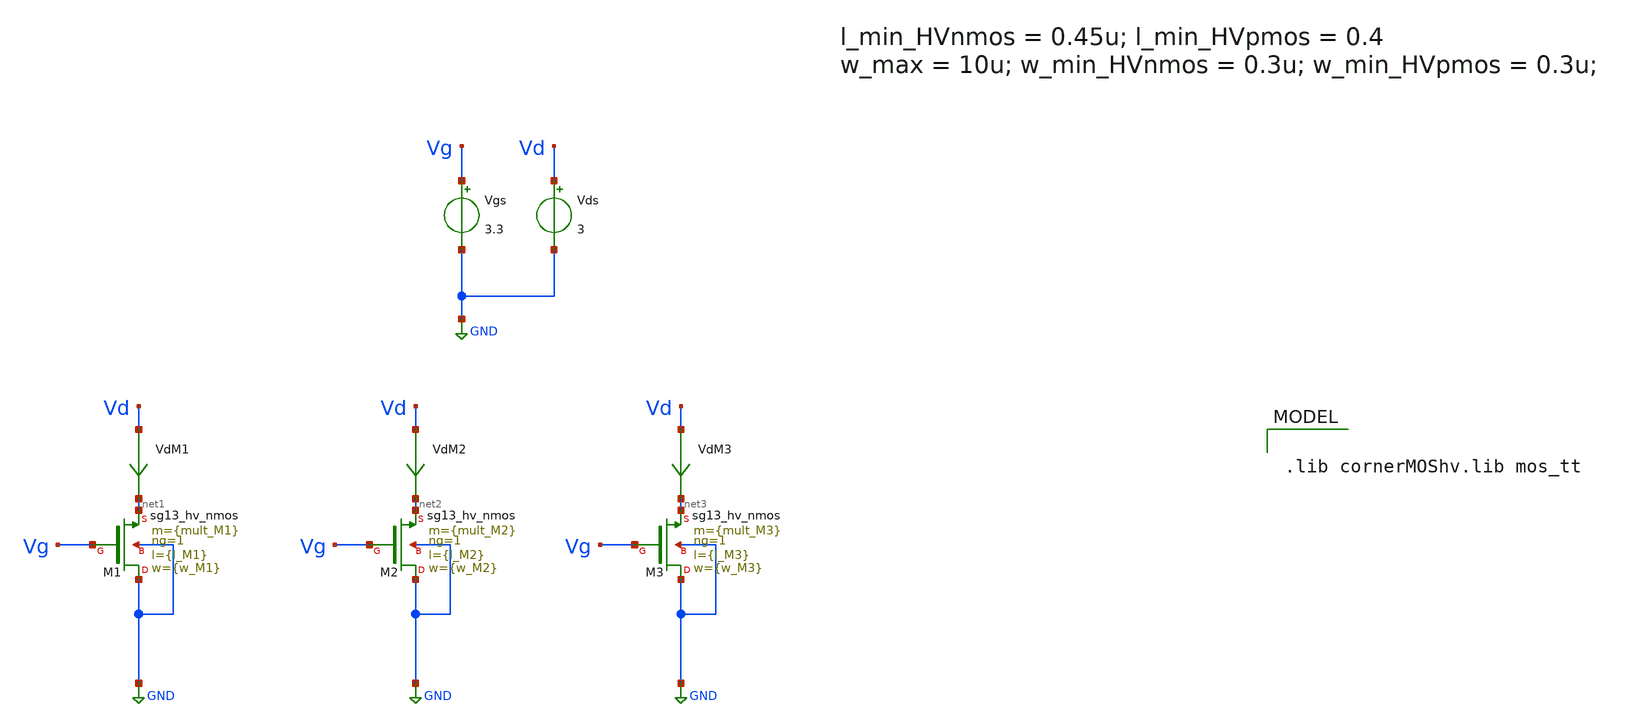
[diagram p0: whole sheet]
** sch_path: xschem/IHP_Tapeout24_AMsent20241028/TB_hvNMOS_charact.sch
**.subckt TB_hvNMOS_charact
XM1 GND Vg net1 GND sg13_hv_nmos w={w_M1} l={l_M1} ng=1 m={mult_M1} mm_ok=1
Vgs Vg GND 3.3
Vds Vd GND 3
VdM1 Vd net1 0
.save i(vdm1)
XM2 GND Vg net2 GND sg13_hv_nmos w={w_M2} l={l_M2} ng=1 m={mult_M2} mm_ok=1
VdM2 Vd net2 0
.save i(vdm2)
XM3 GND Vg net3 GND sg13_hv_nmos w={w_M3} l={l_M3} ng=1 m={mult_M3} mm_ok=1
VdM3 Vd net3 0
.save i(vdm3)
**** begin user architecture code


.param temp=27
.param mult_M1 = 1200
.param w_M1 =10u
.param l_M1 =0.45u

.param mult_M2 = 1200
.param w_M2 =10u
.param l_M2 =0.55u

.param mult_M3 = 1200
.param w_M3 =10u
.param l_M3 =0.65u

.save all
* + @M.XM1.m1[id]  @n.xm1.nsg13_hv_nmos[vth]  @n.xm1.nsg13_hv_nmos[gds]  @n.xm2.nsg13_hv_nmos[vth]
*+  @n.xm2.nsg13_hv_nmos[gds]  @n.xm3.nsg13_hv_nmos[vth]  @n.xm3.nsg13_hv_nmos[gds]  @n.xm1.nsg13_hv_nmos[ad]

.control
*dc Vds 0 3 0.01 Vgs 0.5 3 0.5
dc Vds 0 3 0.01
*dc Vds 0 0.5 0.01
*dc Vds 0 0.5 0.01 temp 0 27 1
write dc_hv_nmos.raw
let G_M1 = @n.xm1.nsg13_hv_nmos[gds]
let G_M2 = @n.xm2.nsg13_hv_nmos[gds]
let G_M3 = @n.xm3.nsg13_hv_nmos[gds]
let Ron_M1 = 1/G_M1
let Ron_M2 = 1/G_M2
let Ron_M3 = 1/G_M3
let Vds = v(Vd)

let Vth_M1 = @n.xm1.nsg13_hv_nmos[vth]
let Vth_M2 = @n.xm2.nsg13_hv_nmos[vth]
let Vth_M3 = @n.xm3.nsg13_hv_nmos[vth]

let Id_M1 = i(VdM1)
plot i(VdM1) i(VdM2) i(VdM3) vs Vds
plot Ron_M1 Ron_M2 Ron_M3 vs Vds
*plot Id_M1
plot Vth_M1 Vth_M2 Vth_M3
*print @n.xm1.nsg13_hv_nmos[vth] @n.xm2.nsg13_hv_nmos[vth] Vth_M1
*print @n.xm2.nsg13_hv_nmos[vth]
write test_nmos.raw




.endc

.control
*dc Vds 0 3 0.01 Vgs 0.5 3 0.5
dc Vds 0 3 0.01
*dc Vds 0 0.5 0.01
*dc Vds 0 0.5 0.01 temp 0 27 1
write dc_hv_nmos.raw
*alter {l_M1} 0.75u
setparam l_M1 = 0.75u
let G_M1 = @n.xm1.nsg13_hv_nmos[gds]
let G_M2 = @n.xm2.nsg13_hv_nmos[gds]
let G_M3 = @n.xm3.nsg13_hv_nmos[gds]
let Ron_M1 = 1/G_M1
let Ron_M2 = 1/G_M2
let Ron_M3 = 1/G_M3
let Vds = v(Vd)

let Vth_M1 = @n.xm1.nsg13_hv_nmos[vth]
let Vth_M2 = @n.xm2.nsg13_hv_nmos[vth]
let Vth_M3 = @n.xm3.nsg13_hv_nmos[vth]

let Id_M1 = i(VdM1)
plot i(VdM1) i(VdM2) i(VdM3) vs Vds
plot Ron_M1 Ron_M2 Ron_M3 vs Vds
*plot Id_M1
plot Vth_M1 Vth_M2 Vth_M3
*print @n.xm1.nsg13_hv_nmos[vth] @n.xm2.nsg13_hv_nmos[vth] Vth_M1
*print @n.xm2.nsg13_hv_nmos[vth]
write test_nmos.raw




.endc



.lib cornerMOShv.lib mos_tt

**** end user architecture code
**.ends
.GLOBAL GND
.end
